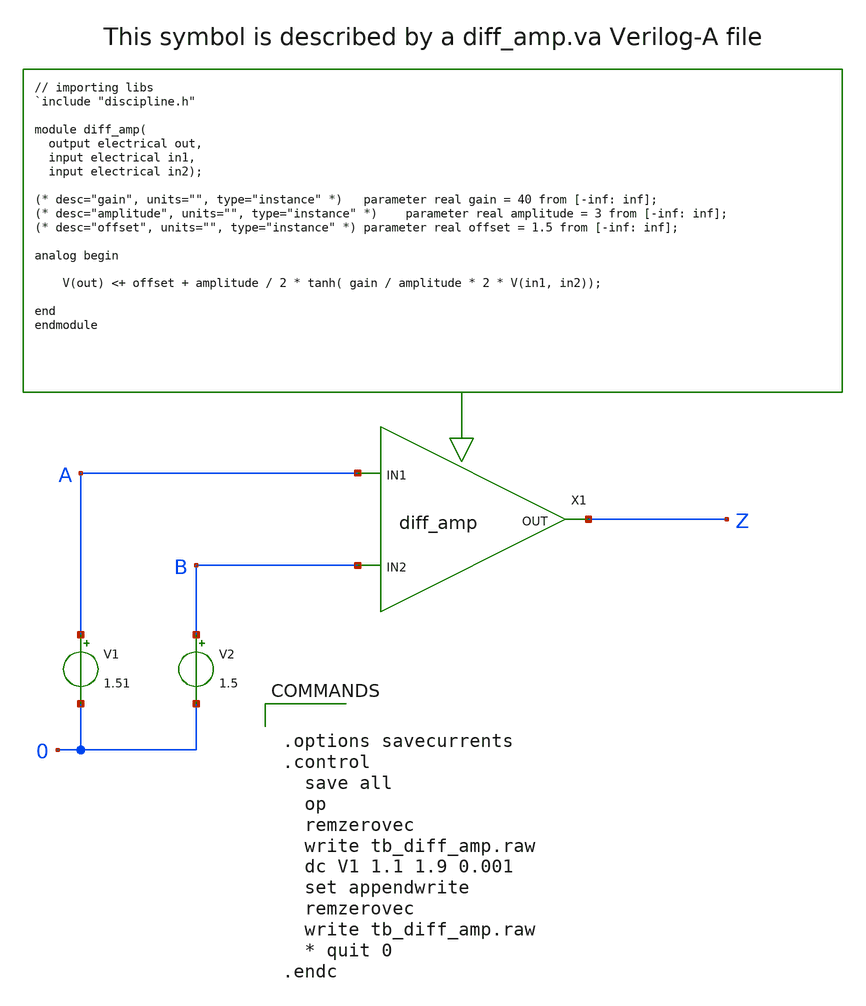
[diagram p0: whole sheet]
** sch_path: xschem_libs_newsym/ngspice/tb_diff_amp/schematic/tb_diff_amp.sch
* Copyright (C) 1998-2024 Stefan Frederik Schippers
* This program is free software; you can redistribute it and/or modify
* it under the terms of the GNU General Public License as published by
* the Free Software Foundation; either version 2 of the License, or
* (at your option) any later version.
* This program is distributed in the hope that it will be useful,
* but WITHOUT ANY WARRANTY; without even the implied warranty of
* MERCHANTABILITY or FITNESS FOR A PARTICULAR PURPOSE.  See the
* GNU General Public License for more details.
* You should have received a copy of the GNU General Public License
* along with this program; if not, write to the Free Software
**.subckt tb_diff_amp
V1 A 0 1.51
V2 B 0 1.5
X1 Z A B diff_amp_cell gain=100 amplitude=5 offset=2.5
**** begin user architecture code


.options savecurrents
.control
  save all
  op
  remzerovec
  write tb_diff_amp.raw
  dc V1 1.1 1.9 0.001
  set appendwrite
  remzerovec
  write tb_diff_amp.raw
  * quit 0
.endc


**** end user architecture code
**.ends
**** begin user architecture code

.control
* following line specifies the location for the .osdi file so ngspice can use it.
pre_osdi [abs_sym_path diff_amp.osdi]
.endc

.model diff_amp_model diff_amp $ gain=40 amplitude=3 offset=1.5

.subckt diff_amp_cell OUT IN1 IN2 gain=40 amplitude=3 offset=1.5
N1 out in1 in2 diff_amp_model gain=gain amplitude=amplitude offset=offset
.ends diff_amp_cell

**** end user architecture code
.end
